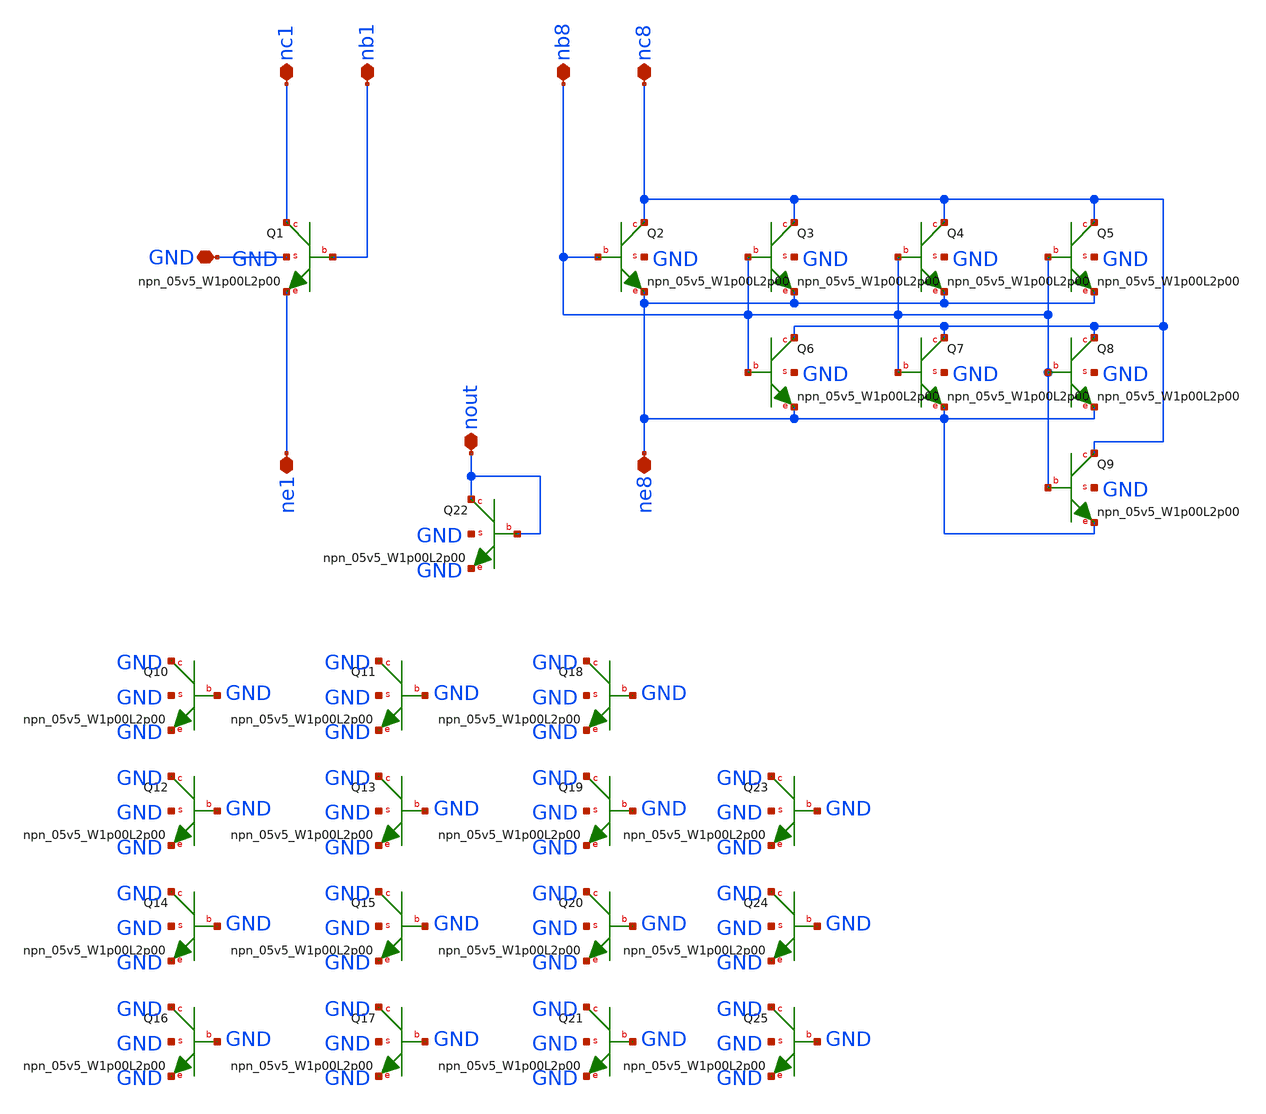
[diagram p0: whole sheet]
** sch_path: xschem/npn_8_1.sch
* Copyright 2021 Stefan Frederik Schippers
* Licensed under the Apache License, Version 2.0 (the "License");
* you may not use this file except in compliance with the License.
* You may obtain a copy of the License at
* https://www.apache.org/licenses/LICENSE-2.0
* Unless required by applicable law or agreed to in writing, software
* distributed under the License is distributed on an "AS IS" BASIS,
* WITHOUT WARRANTIES OR CONDITIONS OF ANY KIND, either express or implied.
* See the License for the specific language governing permissions and
* limitations under the License.
**.subckt npn_8_1 GND nc1 nb1 nb8 nc8 ne8 ne1 nout
*.iopin GND
*.iopin nc1
*.iopin nb1
*.iopin nb8
*.iopin nc8
*.iopin ne8
*.iopin ne1
*.iopin nout
XQ1 nc1 nb1 ne1 GND sky130_fd_pr__npn_05v5_W1p00L2p00
XQ2 nc8 nb8 ne8 GND sky130_fd_pr__npn_05v5_W1p00L2p00
XQ3 nc8 nb8 ne8 GND sky130_fd_pr__npn_05v5_W1p00L2p00
XQ4 nc8 nb8 ne8 GND sky130_fd_pr__npn_05v5_W1p00L2p00
XQ5 nc8 nb8 ne8 GND sky130_fd_pr__npn_05v5_W1p00L2p00
XQ6 nc8 nb8 ne8 GND sky130_fd_pr__npn_05v5_W1p00L2p00
XQ7 nc8 nb8 ne8 GND sky130_fd_pr__npn_05v5_W1p00L2p00
XQ8 nc8 nb8 ne8 GND sky130_fd_pr__npn_05v5_W1p00L2p00
XQ9 nc8 nb8 ne8 GND sky130_fd_pr__npn_05v5_W1p00L2p00
XQ22 nout nout GND GND sky130_fd_pr__npn_05v5_W1p00L2p00
XQ10 GND GND GND GND sky130_fd_pr__npn_05v5_W1p00L2p00
XQ11 GND GND GND GND sky130_fd_pr__npn_05v5_W1p00L2p00
XQ12 GND GND GND GND sky130_fd_pr__npn_05v5_W1p00L2p00
XQ13 GND GND GND GND sky130_fd_pr__npn_05v5_W1p00L2p00
XQ14 GND GND GND GND sky130_fd_pr__npn_05v5_W1p00L2p00
XQ15 GND GND GND GND sky130_fd_pr__npn_05v5_W1p00L2p00
XQ16 GND GND GND GND sky130_fd_pr__npn_05v5_W1p00L2p00
XQ17 GND GND GND GND sky130_fd_pr__npn_05v5_W1p00L2p00
XQ18 GND GND GND GND sky130_fd_pr__npn_05v5_W1p00L2p00
XQ19 GND GND GND GND sky130_fd_pr__npn_05v5_W1p00L2p00
XQ20 GND GND GND GND sky130_fd_pr__npn_05v5_W1p00L2p00
XQ21 GND GND GND GND sky130_fd_pr__npn_05v5_W1p00L2p00
XQ23 GND GND GND GND sky130_fd_pr__npn_05v5_W1p00L2p00
XQ24 GND GND GND GND sky130_fd_pr__npn_05v5_W1p00L2p00
XQ25 GND GND GND GND sky130_fd_pr__npn_05v5_W1p00L2p00
**.ends
.end
